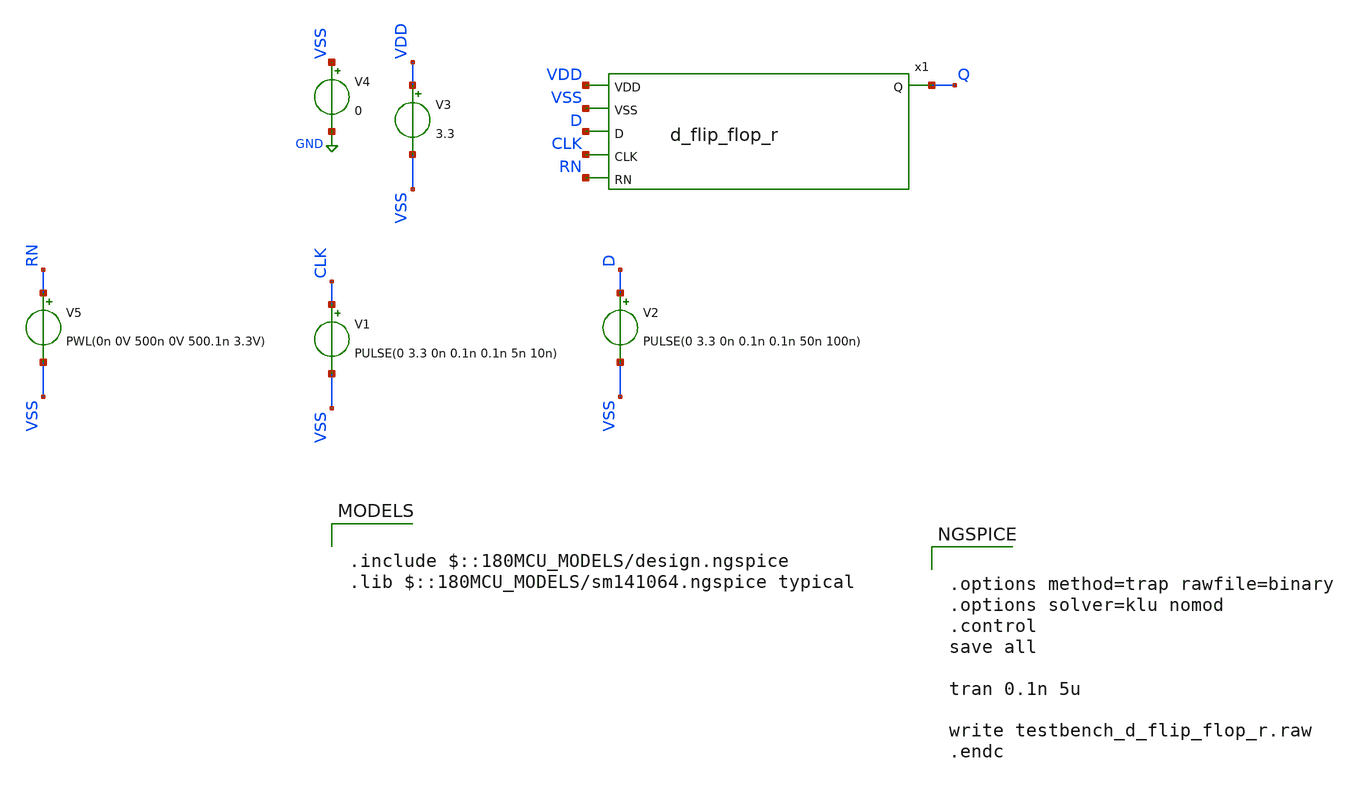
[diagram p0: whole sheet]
** sch_path: designs/libs/tb_digital/tb_d_flip_flop/testbench_d_flip_flop_r.sch
**.subckt testbench_d_flip_flop_r
V1 CLK VSS PULSE(0 3.3 0n 0.1n 0.1n 5n 10n)
V2 D VSS PULSE(0 3.3 0n 0.1n 0.1n 50n 100n)
V3 VDD VSS 3.3
V4 VSS GND 0
V5 RN VSS PWL(0n 0V 500n 0V 500.1n 3.3V)
x1 VDD VSS Q D CLK RN d_flip_flop_r
**** begin user architecture code

.include $::180MCU_MODELS/design.ngspice
.lib $::180MCU_MODELS/sm141064.ngspice typical



.options method=trap rawfile=binary
.options solver=klu nomod
.control
save all

tran 0.1n 5u

write testbench_d_flip_flop_r.raw
.endc


**** end user architecture code
**.ends
.GLOBAL GND
.end
